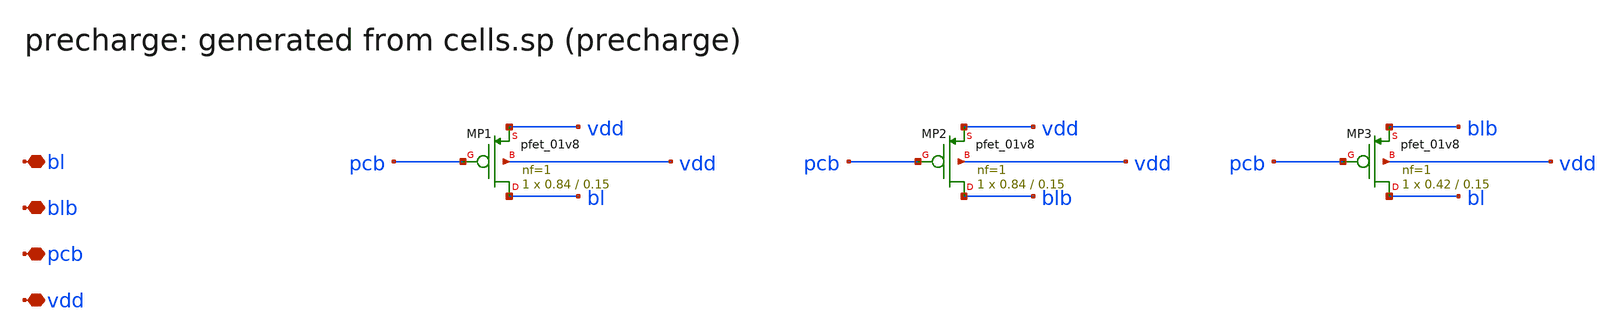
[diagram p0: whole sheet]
** sch_path: sram/xschem/precharge.sch
**.subckt precharge bl blb pcb vdd
*.iopin bl
*.iopin blb
*.iopin pcb
*.iopin vdd
XMP1 bl pcb vdd vdd sky130_fd_pr__pfet_01v8 L=0.15 W=0.84 nf=1 ad='int((nf+1)/2) * W/nf * 0.29' as='int((nf+2)/2) * W/nf * 0.29'
+ pd='2*int((nf+1)/2) * (W/nf + 0.29)' ps='2*int((nf+2)/2) * (W/nf + 0.29)' nrd='0.29 / W' nrs='0.29 / W'
+ sa=0 sb=0 sd=0 mult=1 m=1
XMP2 blb pcb vdd vdd sky130_fd_pr__pfet_01v8 L=0.15 W=0.84 nf=1 ad='int((nf+1)/2) * W/nf * 0.29' as='int((nf+2)/2) * W/nf * 0.29'
+ pd='2*int((nf+1)/2) * (W/nf + 0.29)' ps='2*int((nf+2)/2) * (W/nf + 0.29)' nrd='0.29 / W' nrs='0.29 / W'
+ sa=0 sb=0 sd=0 mult=1 m=1
XMP3 bl pcb blb vdd sky130_fd_pr__pfet_01v8 L=0.15 W=0.42 nf=1 ad='int((nf+1)/2) * W/nf * 0.29' as='int((nf+2)/2) * W/nf * 0.29'
+ pd='2*int((nf+1)/2) * (W/nf + 0.29)' ps='2*int((nf+2)/2) * (W/nf + 0.29)' nrd='0.29 / W' nrs='0.29 / W'
+ sa=0 sb=0 sd=0 mult=1 m=1
**.ends
.end
